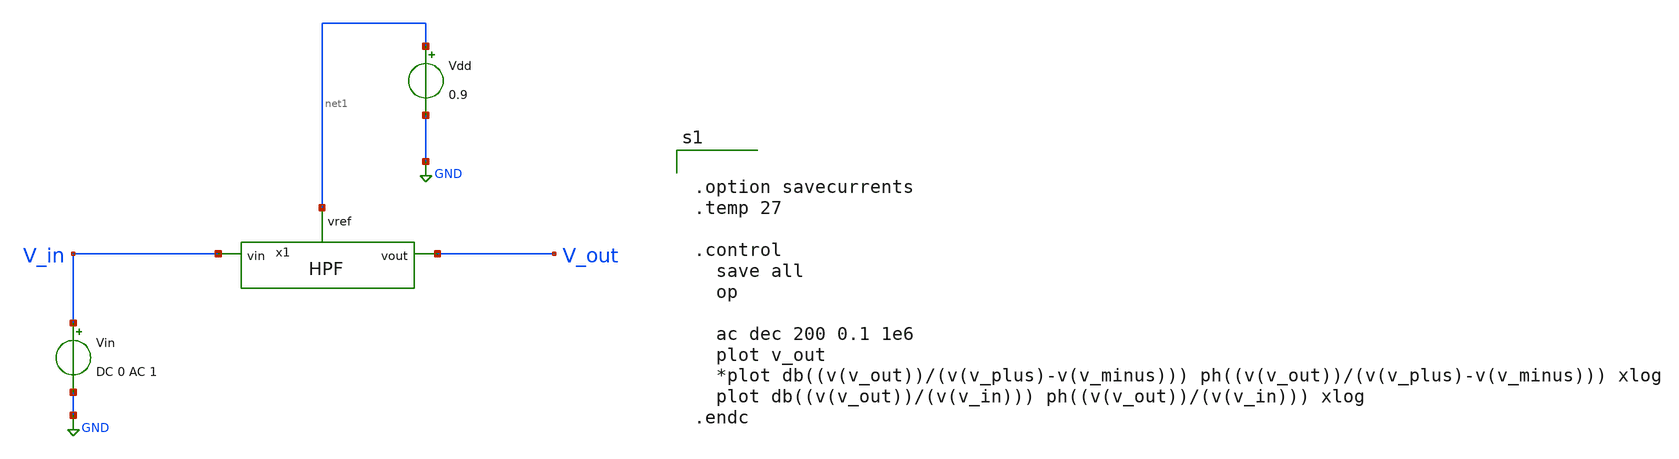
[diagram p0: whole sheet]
** sch_path: Schematic/HPF_AC_tb.sch
**.subckt HPF_AC_tb
Vin V_in GND DC 0 AC 1
Vdd net1 GND 0.9
x1 net1 V_out V_in HPF
**** begin user architecture code


.option savecurrents
.temp 27

.control
  save all
  op

  ac dec 200 0.1 1e6
  plot v_out
  *plot db((v(v_out))/(v(v_plus)-v(v_minus))) ph((v(v_out))/(v(v_plus)-v(v_minus))) xlog
  plot db((v(v_out))/(v(v_in))) ph((v(v_out))/(v(v_in))) xlog
.endc




** opencircuitdesign pdks install
.lib $::SKYWATER_MODELS/sky130.lib.spice tt


**** end user architecture code
**.ends

* expanding   symbol:  /foss/designs/Analog_to_Spike/Schematic/HPF.sym # of pins=3
** sym_path: Schematic/HPF.sym
** sch_path: Schematic/HPF.sch
.subckt HPF vref vout vin
*.ipin vin
*.opin vout
*.ipin vref
XC1 vout vin sky130_fd_pr__cap_mim_m3_1 W=12 L=12 MF=2 m=2
XM1 vout net1 net1 vref sky130_fd_pr__pfet_01v8 L=1 W=1 nf=1 ad='int((nf+1)/2) * W/nf * 0.29' as='int((nf+2)/2) * W/nf * 0.29'
+ pd='2*int((nf+1)/2) * (W/nf + 0.29)' ps='2*int((nf+2)/2) * (W/nf + 0.29)' nrd='0.29 / W' nrs='0.29 / W'
+ sa=0 sb=0 sd=0 mult=1 m=1
XM2 net1 net1 vref vref sky130_fd_pr__pfet_01v8 L=1 W=1 nf=1 ad='int((nf+1)/2) * W/nf * 0.29' as='int((nf+2)/2) * W/nf * 0.29'
+ pd='2*int((nf+1)/2) * (W/nf + 0.29)' ps='2*int((nf+2)/2) * (W/nf + 0.29)' nrd='0.29 / W' nrs='0.29 / W'
+ sa=0 sb=0 sd=0 mult=1 m=1
.ends

.GLOBAL GND
.end
